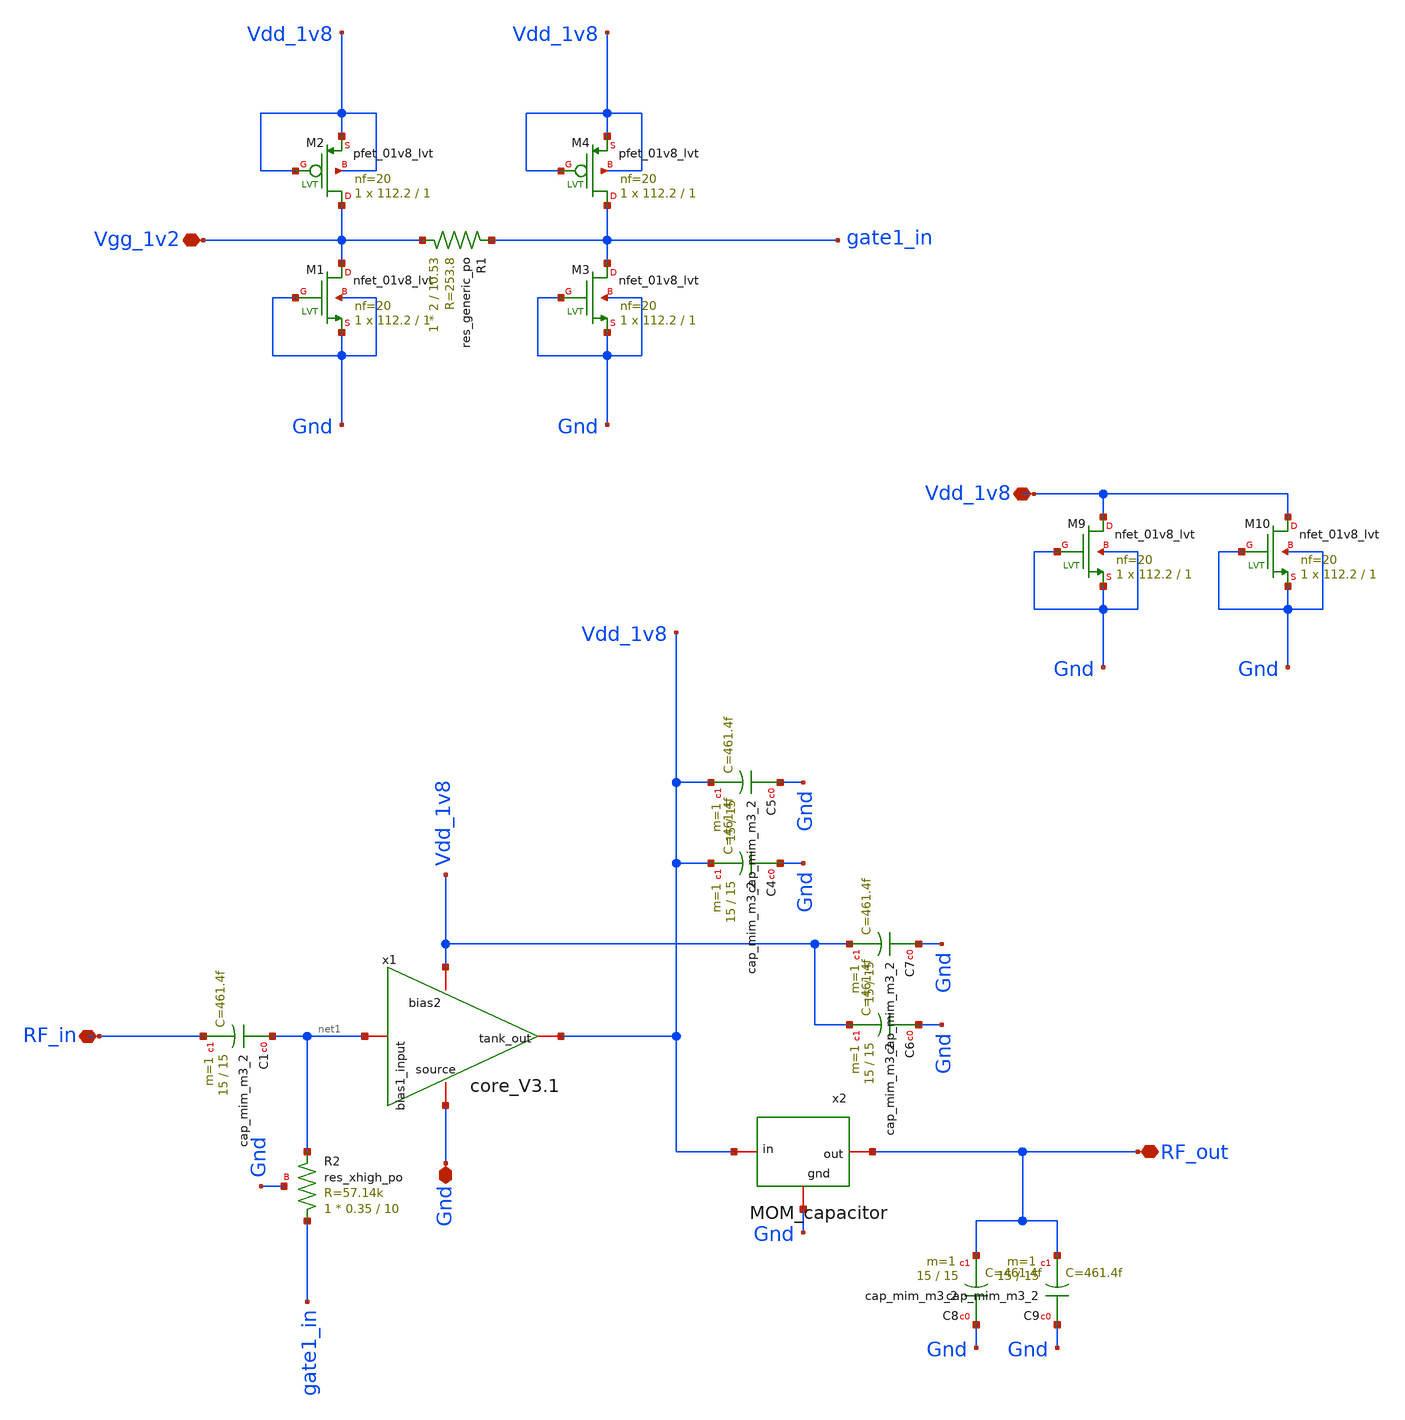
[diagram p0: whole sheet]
** sch_path: LNA_Vband/xschem/LNA_final.sch
**.subckt LNA_final RF_in Gnd RF_out Vdd_1v8 Vgg_1v2
*.iopin RF_in
*.iopin Gnd
*.iopin RF_out
*.iopin Vdd_1v8
*.iopin Vgg_1v2
XC1 net1 RF_in sky130_fd_pr__cap_mim_m3_2 W=15 L=15 MF=1 m=1
XC4 Gnd Vdd_1v8 sky130_fd_pr__cap_mim_m3_2 W=15 L=15 MF=1 m=1
XC5 Gnd Vdd_1v8 sky130_fd_pr__cap_mim_m3_2 W=15 L=15 MF=1 m=1
XC6 Gnd Vdd_1v8 sky130_fd_pr__cap_mim_m3_2 W=15 L=15 MF=1 m=1
XC7 Gnd Vdd_1v8 sky130_fd_pr__cap_mim_m3_2 W=15 L=15 MF=1 m=1
XC8 Gnd RF_out sky130_fd_pr__cap_mim_m3_2 W=15 L=15 MF=1 m=1
XC9 Gnd RF_out sky130_fd_pr__cap_mim_m3_2 W=15 L=15 MF=1 m=1
XM1 Vgg_1v2 Gnd Gnd Gnd sky130_fd_pr__nfet_01v8_lvt L=1 W=112.2 nf=20 ad='int((nf+1)/2) * W/nf * 0.29'
+ as='int((nf+2)/2) * W/nf * 0.29' pd='2*int((nf+1)/2) * (W/nf + 0.29)' ps='2*int((nf+2)/2) * (W/nf + 0.29)'
+ nrd='0.29 / W' nrs='0.29 / W' sa=0 sb=0 sd=0 mult=1 m=1
XM2 Vgg_1v2 Vdd_1v8 Vdd_1v8 Vdd_1v8 sky130_fd_pr__pfet_01v8_lvt L=1 W=112.2 nf=20 ad='int((nf+1)/2) * W/nf * 0.29'
+ as='int((nf+2)/2) * W/nf * 0.29' pd='2*int((nf+1)/2) * (W/nf + 0.29)' ps='2*int((nf+2)/2) * (W/nf + 0.29)'
+ nrd='0.29 / W' nrs='0.29 / W' sa=0 sb=0 sd=0 mult=1 m=1
XR1 Vgg_1v2 gate1_in sky130_fd_pr__res_generic_po W=2 L=10.53 m=1
XM3 gate1_in Gnd Gnd Gnd sky130_fd_pr__nfet_01v8_lvt L=1 W=112.2 nf=20 ad='int((nf+1)/2) * W/nf * 0.29'
+ as='int((nf+2)/2) * W/nf * 0.29' pd='2*int((nf+1)/2) * (W/nf + 0.29)' ps='2*int((nf+2)/2) * (W/nf + 0.29)'
+ nrd='0.29 / W' nrs='0.29 / W' sa=0 sb=0 sd=0 mult=1 m=1
XM4 gate1_in Vdd_1v8 Vdd_1v8 Vdd_1v8 sky130_fd_pr__pfet_01v8_lvt L=1 W=112.2 nf=20 ad='int((nf+1)/2) * W/nf * 0.29'
+ as='int((nf+2)/2) * W/nf * 0.29' pd='2*int((nf+1)/2) * (W/nf + 0.29)' ps='2*int((nf+2)/2) * (W/nf + 0.29)'
+ nrd='0.29 / W' nrs='0.29 / W' sa=0 sb=0 sd=0 mult=1 m=1
XM9 Vdd_1v8 Gnd Gnd Gnd sky130_fd_pr__nfet_01v8_lvt L=1 W=112.2 nf=20 ad='int((nf+1)/2) * W/nf * 0.29'
+ as='int((nf+2)/2) * W/nf * 0.29' pd='2*int((nf+1)/2) * (W/nf + 0.29)' ps='2*int((nf+2)/2) * (W/nf + 0.29)'
+ nrd='0.29 / W' nrs='0.29 / W' sa=0 sb=0 sd=0 mult=1 m=1
XM10 Vdd_1v8 Gnd Gnd Gnd sky130_fd_pr__nfet_01v8_lvt L=1 W=112.2 nf=20 ad='int((nf+1)/2) * W/nf * 0.29'
+ as='int((nf+2)/2) * W/nf * 0.29' pd='2*int((nf+1)/2) * (W/nf + 0.29)' ps='2*int((nf+2)/2) * (W/nf + 0.29)'
+ nrd='0.29 / W' nrs='0.29 / W' sa=0 sb=0 sd=0 mult=1 m=1
x2 RF_out Vdd_1v8 Gnd MOM_capacitor
x1 Vdd_1v8 Vdd_1v8 net1 Gnd core_V3.1
XR2 gate1_in net1 Gnd sky130_fd_pr__res_xhigh_po W=0.35 L=10 mult=1 m=1
**.ends
.end
